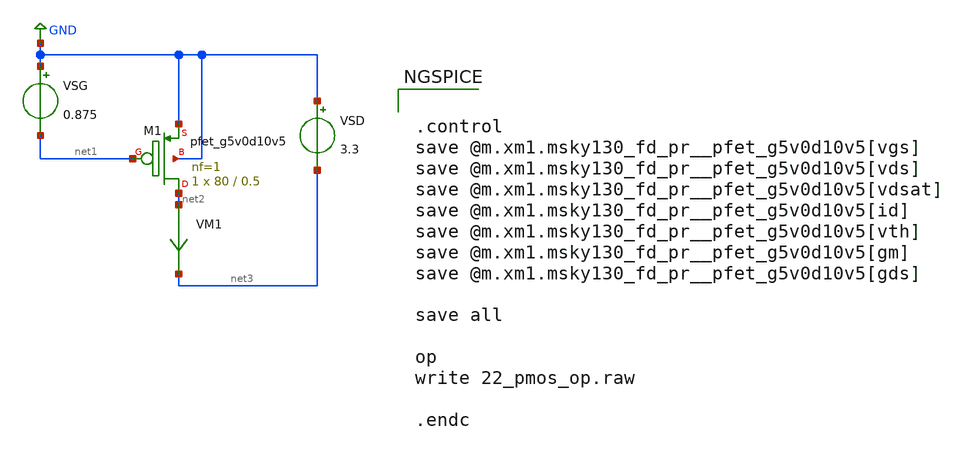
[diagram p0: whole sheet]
** sch_path: xschem/help/22_pmos_op.sch
**.subckt 22_pmos_op
VSG GND net1 0.875
VSD GND net3 3.3
VM1 net2 net3 0
.save i(vm1)
XM1 net2 net1 GND GND sky130_fd_pr__pfet_g5v0d10v5 L=0.5 W=80 nf=1 ad='int((nf+1)/2) * W/nf * 0.29' as='int((nf+2)/2) * W/nf * 0.29'
+ pd='2*int((nf+1)/2) * (W/nf + 0.29)' ps='2*int((nf+2)/2) * (W/nf + 0.29)' nrd='0.29 / W' nrs='0.29 / W'
+ sa=0 sb=0 sd=0 mult=1 m=1
**** begin user architecture code

** opencircuitdesign pdks install
.lib $::SKYWATER_MODELS/sky130.lib.spice tt




.control
save @m.xm1.msky130_fd_pr__pfet_g5v0d10v5[vgs]
save @m.xm1.msky130_fd_pr__pfet_g5v0d10v5[vds]
save @m.xm1.msky130_fd_pr__pfet_g5v0d10v5[vdsat]
save @m.xm1.msky130_fd_pr__pfet_g5v0d10v5[id]
save @m.xm1.msky130_fd_pr__pfet_g5v0d10v5[vth]
save @m.xm1.msky130_fd_pr__pfet_g5v0d10v5[gm]
save @m.xm1.msky130_fd_pr__pfet_g5v0d10v5[gds]

save all

op
write 22_pmos_op.raw

.endc


**** end user architecture code
**.ends
.GLOBAL GND
.end
